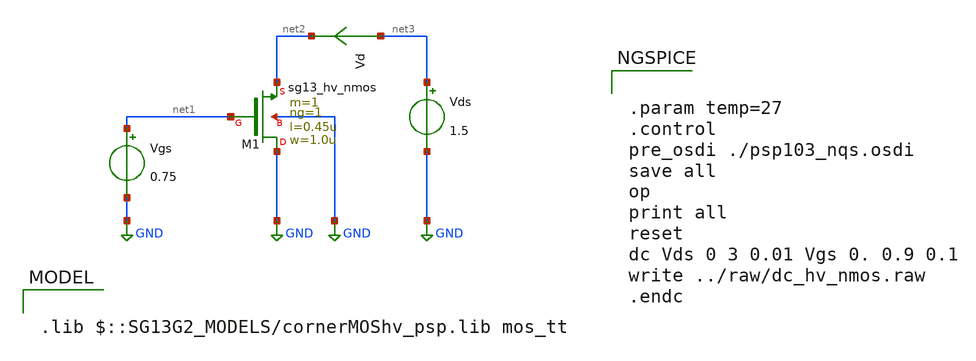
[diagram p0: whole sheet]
** sch_path: ihp-sg13g2/libs.tech/xschem/sg13g2_tests/dc_hv_nmos.sch
* Copyright 2023 IHP PDK Authors
**.subckt dc_hv_nmos
Vgs net1 GND 0.75
Vds net3 GND 1.5
XM1 GND net1 net2 GND sg13_hv_nmos w=1.0u l=0.45u ng=1 m=1 mm_ok=1
Vd net3 net2 0
.save i(vd)
**** begin user architecture code

.lib $::SG13G2_MODELS/cornerMOShv_psp.lib mos_tt



.param temp=27
.control
pre_osdi ./psp103_nqs.osdi
save all
op
print all
reset
dc Vds 0 3 0.01 Vgs 0. 0.9 0.1
write ../raw/dc_hv_nmos.raw
.endc


**** end user architecture code
**.ends
.GLOBAL GND
.end
